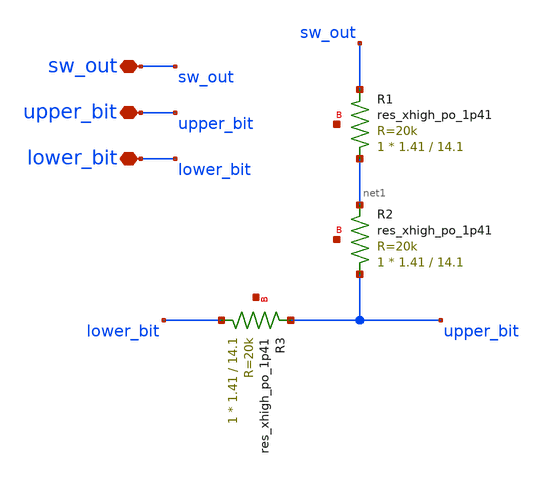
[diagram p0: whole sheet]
** sch_path: xschem/uc_res_x3/uc_res_x3.sch
**.subckt uc_res_x3 sw_out upper_bit lower_bit
*.iopin sw_out
*.iopin upper_bit
*.iopin lower_bit
XR1 net1 sw_out net2 sky130_fd_pr__res_xhigh_po_1p41 L=14.1 mult=1 m=1
XR2 upper_bit net1 net3 sky130_fd_pr__res_xhigh_po_1p41 L=14.1 mult=1 m=1
XR3 lower_bit upper_bit net4 sky130_fd_pr__res_xhigh_po_1p41 L=14.1 mult=1 m=1
**.ends
.end
